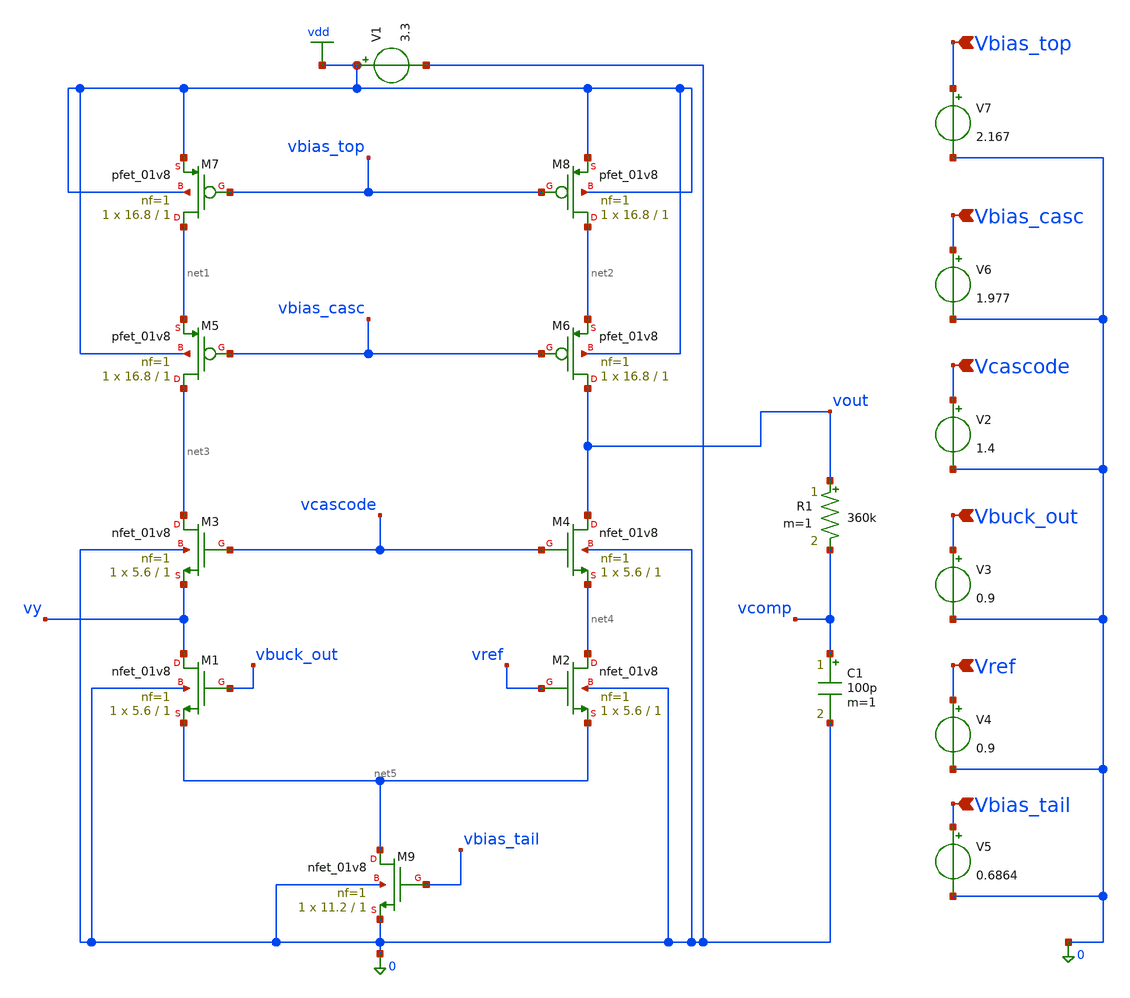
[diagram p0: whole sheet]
** sch_path: telescopic_amp.sch
**.subckt telescopic_amp Vcascode Vbuck_out Vref Vbias_tail Vbias_casc Vbias_top
*.ipin Vcascode
*.ipin Vbuck_out
*.ipin Vref
*.ipin Vbias_tail
*.ipin Vbias_casc
*.ipin Vbias_top
XM3 net3 vcascode vy 0 sky130_fd_pr__nfet_01v8 L=1 W=5.6 nf=1 ad='int((1 + 1)/2) * 5.6 / 1 * 0.29' as='int((1 + 2)/2) * 5.6 / 1 * 0.29'
+ pd='2*int((1 + 1)/2) * (5.6 / 1 + 0.29)' ps='2*int((1 + 2)/2) * (5.6 / 1 + 0.29)' nrd='0.29 / 5.6 ' nrs='0.29 / 5.6 '
+ sa=0 sb=0 sd=0 mult=1 m=1
XM8 net2 vbias_top vdd vdd sky130_fd_pr__pfet_01v8 L=1 W=16.8 nf=1 ad='int((1 + 1)/2) * 16.8 / 1 * 0.29'
+ as='int((1 + 2)/2) * 16.8 / 1 * 0.29' pd='2*int((1 + 1)/2) * (16.8 / 1 + 0.29)' ps='2*int((1 + 2)/2) * (16.8 / 1 + 0.29)'
+ nrd='0.29 / 16.8 ' nrs='0.29 / 16.8 ' sa=0 sb=0 sd=0 mult=1 m=1
XM7 net1 vbias_top vdd vdd sky130_fd_pr__pfet_01v8 L=1 W=16.8 nf=1 ad='int((1 + 1)/2) * 16.8 / 1 * 0.29'
+ as='int((1 + 2)/2) * 16.8 / 1 * 0.29' pd='2*int((1 + 1)/2) * (16.8 / 1 + 0.29)' ps='2*int((1 + 2)/2) * (16.8 / 1 + 0.29)'
+ nrd='0.29 / 16.8 ' nrs='0.29 / 16.8 ' sa=0 sb=0 sd=0 mult=1 m=1
XM5 net3 vbias_casc net1 vdd sky130_fd_pr__pfet_01v8 L=1 W=16.8 nf=1 ad='int((1 + 1)/2) * 16.8 / 1 * 0.29'
+ as='int((1 + 2)/2) * 16.8 / 1 * 0.29' pd='2*int((1 + 1)/2) * (16.8 / 1 + 0.29)' ps='2*int((1 + 2)/2) * (16.8 / 1 + 0.29)'
+ nrd='0.29 / 16.8 ' nrs='0.29 / 16.8 ' sa=0 sb=0 sd=0 mult=1 m=1
XM6 vout vbias_casc net2 vdd sky130_fd_pr__pfet_01v8 L=1 W=16.8 nf=1 ad='int((1 + 1)/2) * 16.8 / 1 * 0.29'
+ as='int((1 + 2)/2) * 16.8 / 1 * 0.29' pd='2*int((1 + 1)/2) * (16.8 / 1 + 0.29)' ps='2*int((1 + 2)/2) * (16.8 / 1 + 0.29)'
+ nrd='0.29 / 16.8 ' nrs='0.29 / 16.8 ' sa=0 sb=0 sd=0 mult=1 m=1
XM1 vy vbuck_out net5 0 sky130_fd_pr__nfet_01v8 L=1 W=5.6 nf=1 ad='int((1 + 1)/2) * 5.6 / 1 * 0.29' as='int((1 + 2)/2) * 5.6 / 1 * 0.29'
+ pd='2*int((1 + 1)/2) * (5.6 / 1 + 0.29)' ps='2*int((1 + 2)/2) * (5.6 / 1 + 0.29)' nrd='0.29 / 5.6 ' nrs='0.29 / 5.6 '
+ sa=0 sb=0 sd=0 mult=1 m=1
XM4 vout vcascode net4 0 sky130_fd_pr__nfet_01v8 L=1 W=5.6 nf=1 ad='int((1 + 1)/2) * 5.6 / 1 * 0.29'
+ as='int((1 + 2)/2) * 5.6 / 1 * 0.29' pd='2*int((1 + 1)/2) * (5.6 / 1 + 0.29)' ps='2*int((1 + 2)/2) * (5.6 / 1 + 0.29)'
+ nrd='0.29 / 5.6 ' nrs='0.29 / 5.6 ' sa=0 sb=0 sd=0 mult=1 m=1
XM2 net4 vref net5 0 sky130_fd_pr__nfet_01v8 L=1 W=5.6 nf=1 ad='int((1 + 1)/2) * 5.6 / 1 * 0.29' as='int((1 + 2)/2) * 5.6 / 1 * 0.29'
+ pd='2*int((1 + 1)/2) * (5.6 / 1 + 0.29)' ps='2*int((1 + 2)/2) * (5.6 / 1 + 0.29)' nrd='0.29 / 5.6 ' nrs='0.29 / 5.6 '
+ sa=0 sb=0 sd=0 mult=1 m=1
XM9 net5 vbias_tail 0 0 sky130_fd_pr__nfet_01v8 L=1 W=11.2 nf=1 ad='int((1 + 1)/2) * 11.2 / 1 * 0.29'
+ as='int((1 + 2)/2) * 11.2 / 1 * 0.29' pd='2*int((1 + 1)/2) * (11.2 / 1 + 0.29)' ps='2*int((1 + 2)/2) * (11.2 / 1 + 0.29)'
+ nrd='0.29 / 11.2 ' nrs='0.29 / 11.2 ' sa=0 sb=0 sd=0 mult=1 m=1
V1 vdd 0 3.3
V2 Vcascode 0 1.4
V3 Vbuck_out 0 0.9
V4 Vref 0 0.9
V5 Vbias_tail 0 0.6864
V6 Vbias_casc 0 1.977
V7 Vbias_top 0 2.167
R1 vout vcomp 360k m=1
C1 vcomp 0 100p m=1
**** begin user architecture code


.lib /home/areebjamal/pdk/volare/sky130/versions/bdc9412b3e468c102d01b7cf6337be06ec6e9c9a/sky130A/libs.tech/ngspice/sky130.lib.spice tt
.control
op
tf v(vout) V4
print transfer_function
.endc


**** end user architecture code
**.ends
.GLOBAL vdd
.end
